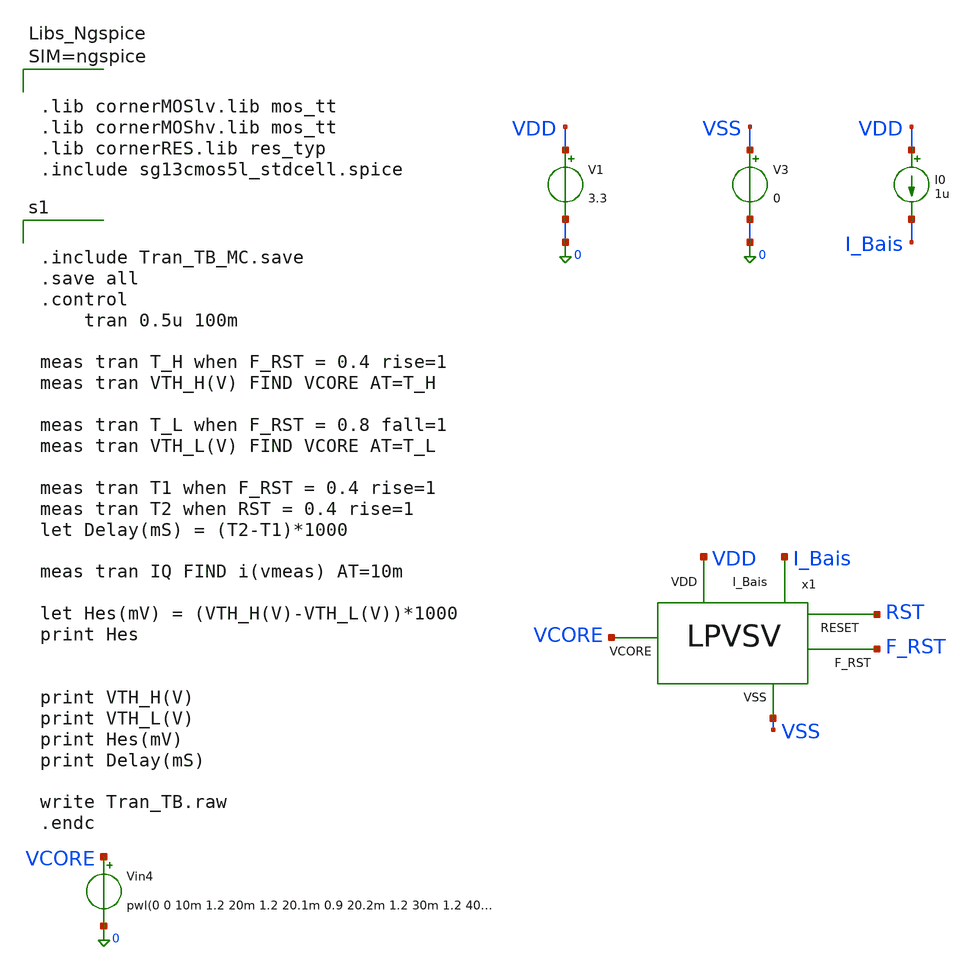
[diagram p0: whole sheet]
** sch_path: Tran_Analysis/Tran_TB.sch
**.subckt Tran_TB
x1 VDD VCORE I_Bais RST F_RST VSS LPVSV
I0 VDD I_Bais 1u
V1 VDD 0 3.3
V3 VSS 0 0
Vin4 VCORE 0 pwl(0 0 10m 1.2 20m 1.2 20.1m 0.9 20.2m 1.2 30m 1.2 40m 0.7 50m 0.7 50.1m 1.2 55m 1.2
+ 55.1m 0.7 60m 0.7 61m 0 70m 0 70.1m 1.2 70.2m 0 80m 0 100m 1)
**** begin user architecture code



.lib cornerMOSlv.lib mos_tt
.lib cornerMOShv.lib mos_tt
.lib cornerRES.lib res_typ
.include sg13cmos5l_stdcell.spice





.include Tran_TB_MC.save
.save all
.control
	tran 0.5u 100m

meas tran T_H when F_RST = 0.4 rise=1
meas tran VTH_H(V) FIND VCORE AT=T_H

meas tran T_L when F_RST = 0.8 fall=1
meas tran VTH_L(V) FIND VCORE AT=T_L

meas tran T1 when F_RST = 0.4 rise=1
meas tran T2 when RST = 0.4 rise=1
let Delay(mS) = (T2-T1)*1000

meas tran IQ FIND i(vmeas) AT=10m

let Hes(mV) = (VTH_H(V)-VTH_L(V))*1000
print Hes


print VTH_H(V)
print VTH_L(V)
print Hes(mV)
print Delay(mS)

write Tran_TB.raw
.endc


**** end user architecture code
**.ends
.end
